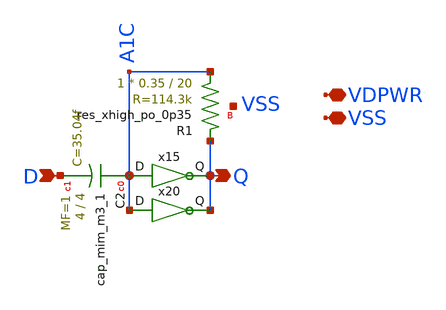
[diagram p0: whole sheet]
** sch_path: xschem/pll_invresfb.sch
**.subckt pll_invresfb Q D VDPWR VSS
*.opin Q
*.ipin D
*.iopin VDPWR
*.iopin VSS
x15 A1C Q VDPWR VSS pll_inv1
XR1 A1C Q VSS sky130_fd_pr__res_xhigh_po_0p35 L=20 mult=1 m=1
XC2 A1C D sky130_fd_pr__cap_mim_m3_1 W=4 L=4 MF=1 m=1
x20 A1C Q VDPWR VSS pll_inv1
**.ends

* expanding   symbol:  pll_inv1.sym # of pins=2
** sym_path: xschem/pll_inv1.sym
** sch_path: xschem/pll_inv1.sch
.subckt pll_inv1 D Q VDD VSS
*.opin Q
*.ipin D
*.ipin VDD
*.ipin VSS
XM3 Q D net1 net1 sky130_fd_pr__pfet_01v8_lvt L=0.5 W=1 nf=1 ad='int((nf+1)/2) * W/nf * 0.29' as='int((nf+2)/2) * W/nf * 0.29'
+ pd='2*int((nf+1)/2) * (W/nf + 0.29)' ps='2*int((nf+2)/2) * (W/nf + 0.29)' nrd='0.29 / W' nrs='0.29 / W'
+ sa=0 sb=0 sd=0 mult=1 m=1
vpwr VDD net1 0
.save i(vpwr)
XM1 Q D VSS VSS sky130_fd_pr__nfet_01v8_lvt L=0.25 W=0.5 nf=1 ad='int((nf+1)/2) * W/nf * 0.29' as='int((nf+2)/2) * W/nf * 0.29'
+ pd='2*int((nf+1)/2) * (W/nf + 0.29)' ps='2*int((nf+2)/2) * (W/nf + 0.29)' nrd='0.29 / W' nrs='0.29 / W'
+ sa=0 sb=0 sd=0 mult=1 m=1
.ends

.end
